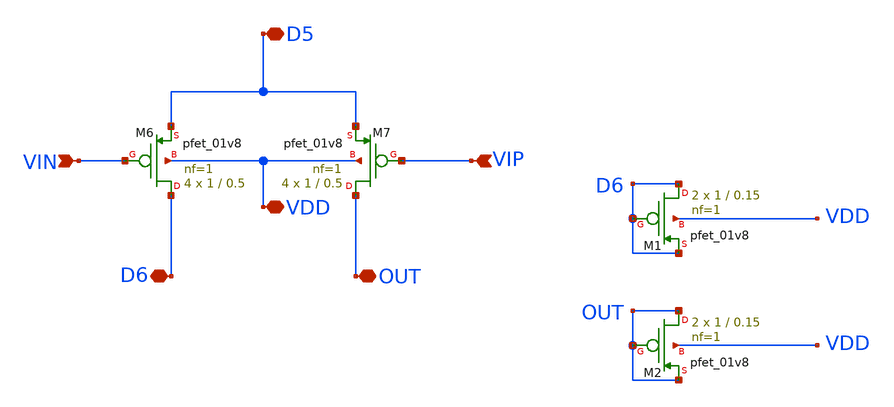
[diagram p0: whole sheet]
** sch_path: PMOS_VIN_VIP_OUT/PMOS_VIN_VIP_OUT.sch
**.subckt PMOS_VIN_VIP_OUT D5 VDD D6 OUT VIP VIN
*.iopin D5
*.iopin VDD
*.iopin D6
*.iopin OUT
*.ipin VIP
*.ipin VIN
XM7 OUT VIP D5 VDD sky130_fd_pr__pfet_01v8 L=0.5 W=1 nf=1 ad='int((nf+1)/2) * W/nf * 0.29' as='int((nf+2)/2) * W/nf * 0.29'
+ pd='2*int((nf+1)/2) * (W/nf + 0.29)' ps='2*int((nf+2)/2) * (W/nf + 0.29)' nrd='0.29 / W' nrs='0.29 / W'
+ sa=0 sb=0 sd=0 mult=4 m=4
XM6 D6 VIN D5 VDD sky130_fd_pr__pfet_01v8 L=0.5 W=1 nf=1 ad='int((nf+1)/2) * W/nf * 0.29' as='int((nf+2)/2) * W/nf * 0.29'
+ pd='2*int((nf+1)/2) * (W/nf + 0.29)' ps='2*int((nf+2)/2) * (W/nf + 0.29)' nrd='0.29 / W' nrs='0.29 / W'
+ sa=0 sb=0 sd=0 mult=4 m=4
XM1 D6 D6 D6 VDD sky130_fd_pr__pfet_01v8 L=0.15 W=1 nf=1 ad='int((nf+1)/2) * W/nf * 0.29' as='int((nf+2)/2) * W/nf * 0.29'
+ pd='2*int((nf+1)/2) * (W/nf + 0.29)' ps='2*int((nf+2)/2) * (W/nf + 0.29)' nrd='0.29 / W' nrs='0.29 / W'
+ sa=0 sb=0 sd=0 mult=2 m=2
XM2 OUT OUT OUT VDD sky130_fd_pr__pfet_01v8 L=0.15 W=1 nf=1 ad='int((nf+1)/2) * W/nf * 0.29' as='int((nf+2)/2) * W/nf * 0.29'
+ pd='2*int((nf+1)/2) * (W/nf + 0.29)' ps='2*int((nf+2)/2) * (W/nf + 0.29)' nrd='0.29 / W' nrs='0.29 / W'
+ sa=0 sb=0 sd=0 mult=2 m=2
**.ends
.end
